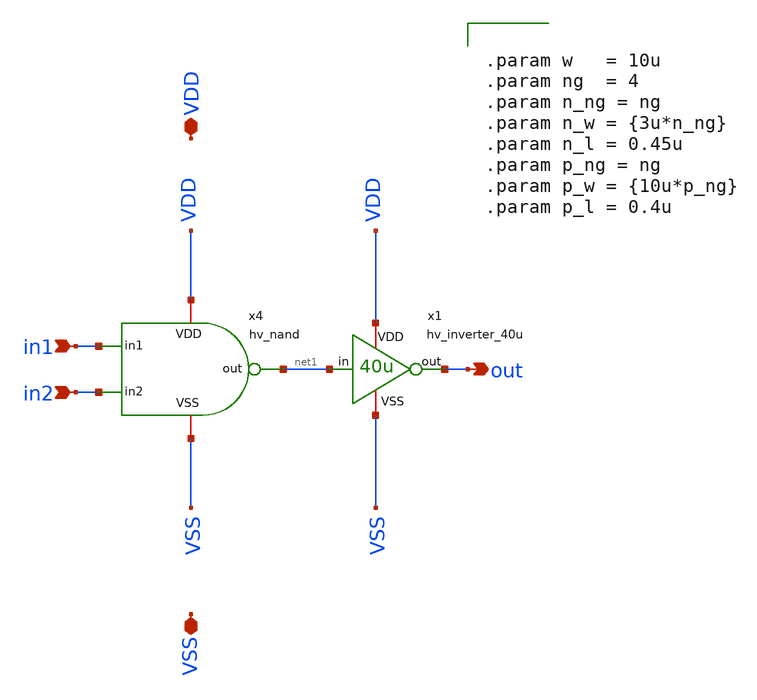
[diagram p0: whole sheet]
** sch_path: macros/heichips26_vcr/macros/switched_capacitor/schematic/xschem/hv_and.sch
**.subckt hv_and in1 VDD VSS out in2
*.ipin in1
*.iopin VDD
*.iopin VSS
*.opin out
*.ipin in2
x4 VDD in1 net1 in2 VSS hv_nand
x1 VDD net1 out VSS hv_inverter_40u
**** begin user architecture code


.param w   = 10u
.param ng  = 4
.param n_ng = ng
.param n_w = {3u*n_ng}
.param n_l = 0.45u
.param p_ng = ng
.param p_w = {10u*p_ng}
.param p_l = 0.4u


**** end user architecture code
**.ends

* expanding   symbol:  hv_nand.sym # of pins=5
** sym_path: macros/heichips26_vcr/macros/switched_capacitor/schematic/xschem/hv_nand.sym
** sch_path: macros/heichips26_vcr/macros/switched_capacitor/schematic/xschem/hv_nand.sch
.subckt hv_nand VDD in1 out in2 VSS
*.ipin in1
*.iopin VDD
*.iopin VSS
*.opin out
*.ipin in2
**** begin user architecture code


.param w   = 10u
.param ng  = 4
.param n_ng = ng
.param n_w = {3u*n_ng}
.param n_l = 0.45u
.param p_ng = ng
.param p_w = {10u*p_ng}
.param p_l = 0.4u


**** end user architecture code
XM2 out in1 net1 VSS sg13_hv_nmos w={n_w} l={n_l} ng={ng} m=1 mm_ok=1
XM3 out in2 VDD VDD sg13_hv_pmos w={p_w} l={p_l} ng={ng} m=1 mm_ok=1
XM1 net1 in2 VSS VSS sg13_hv_nmos w={n_w} l={n_l} ng={ng} m=1 mm_ok=1
XM4 out in1 VDD VDD sg13_hv_pmos w={p_w} l={p_l} ng={ng} m=1 mm_ok=1
.ends


* expanding   symbol:  hv_inverter_40u.sym # of pins=4
** sym_path: macros/heichips26_vcr/macros/switched_capacitor/schematic/xschem/hv_inverter_40u.sym
** sch_path: macros/heichips26_vcr/macros/switched_capacitor/schematic/xschem/hv_inverter_40u.sch
.subckt hv_inverter_40u VDD in out VSS
*.ipin in
*.iopin VDD
*.iopin VSS
*.opin out
XM2 out in VSS VSS sg13_hv_nmos w={n_w} l={n_l} ng={ng} m=1 mm_ok=1
XM3 out in VDD VDD sg13_hv_pmos w={p_w} l={p_l} ng={ng} m=1 mm_ok=1
**** begin user architecture code


.param w   = 10u
.param ng  = 4
.param n_ng = ng
.param n_w = {3u*n_ng}
.param n_l = 0.45u
.param p_ng = ng
.param p_w = {10u*p_ng}
.param p_l = 0.4u


**** end user architecture code
.ends

.end
